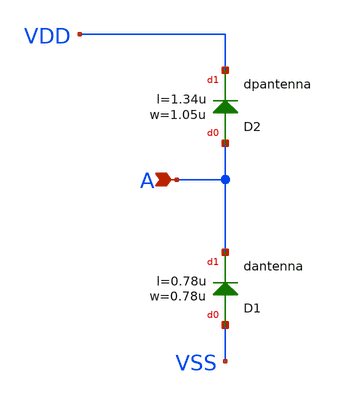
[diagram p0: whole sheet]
** sch_path: ihp-sg13g2/libs.ref/sg13g2_stdcell_hv/sch/xschem/sg13g2_hv_antennanp.sch
**.subckt sg13g2_hv_antennanp A
*.ipin A
XD1 VSS A dantenna l=0.78u w=0.78u
XD2 A VDD dpantenna l=1.34u w=1.05u
**.ends
.end
